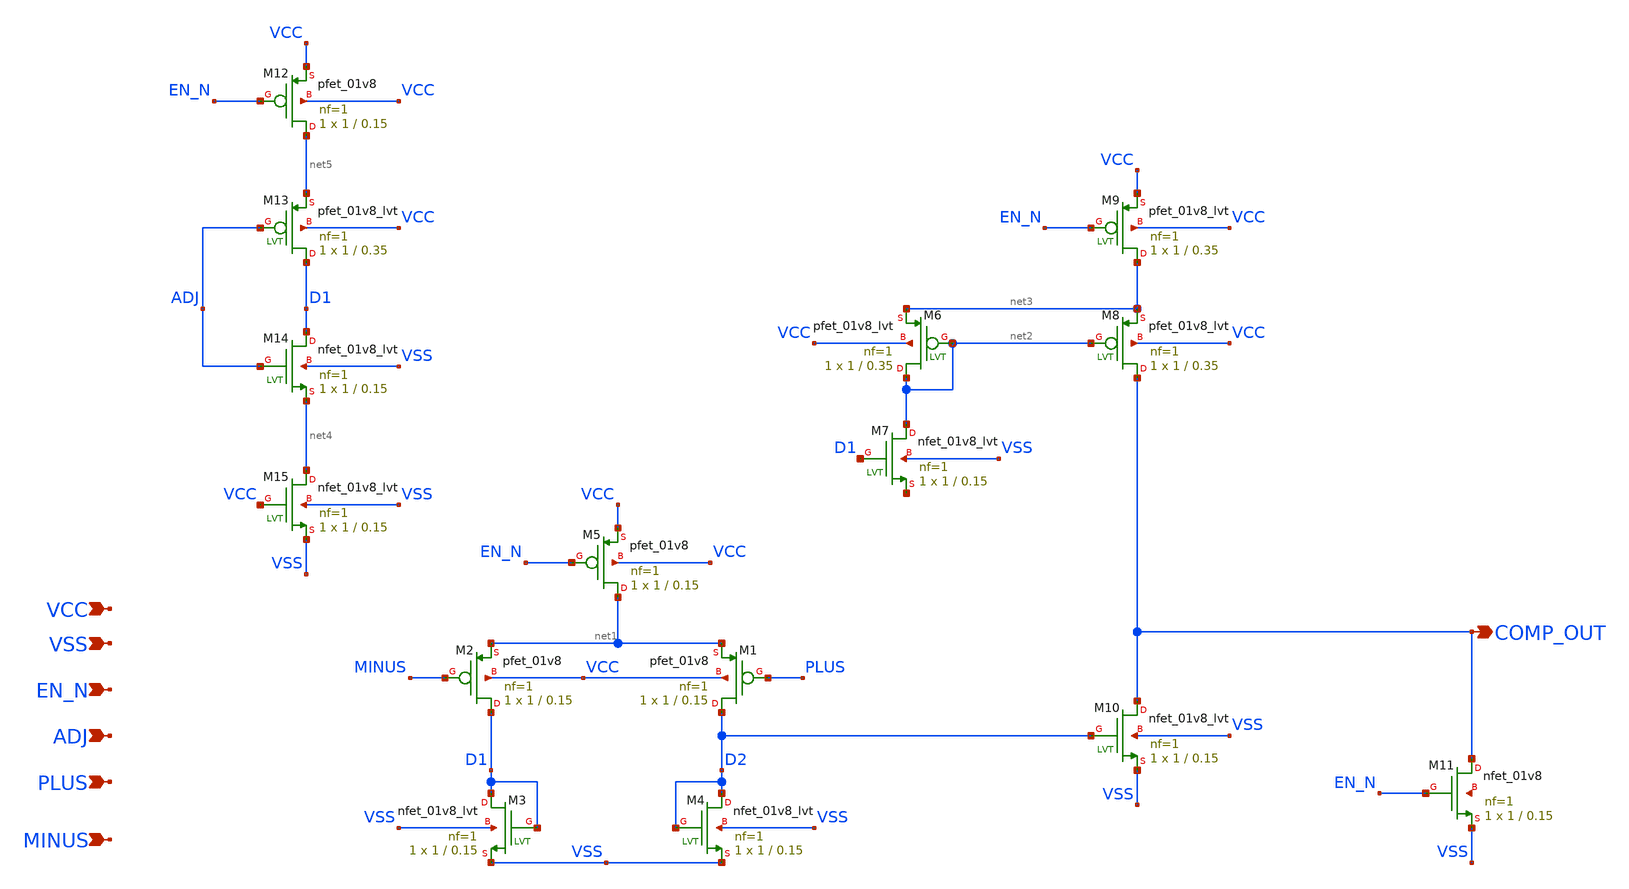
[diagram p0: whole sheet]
** sch_path: xschem/comparator.sch
**.subckt comparator VCC VSS EN_N ADJ PLUS MINUS COMP_OUT
*.ipin VCC
*.ipin VSS
*.ipin EN_N
*.ipin ADJ
*.ipin PLUS
*.ipin MINUS
*.opin COMP_OUT
XM1 D2 PLUS net1 VCC sky130_fd_pr__pfet_01v8 L=0.15 W=1 nf=1 ad='int((nf+1)/2) * W/nf * 0.29' as='int((nf+2)/2) * W/nf * 0.29'
+ pd='2*int((nf+1)/2) * (W/nf + 0.29)' ps='2*int((nf+2)/2) * (W/nf + 0.29)' nrd='0.29 / W' nrs='0.29 / W'
+ sa=0 sb=0 sd=0 mult=1 m=1
XM2 D1 MINUS net1 VCC sky130_fd_pr__pfet_01v8 L=0.15 W=1 nf=1 ad='int((nf+1)/2) * W/nf * 0.29' as='int((nf+2)/2) * W/nf * 0.29'
+ pd='2*int((nf+1)/2) * (W/nf + 0.29)' ps='2*int((nf+2)/2) * (W/nf + 0.29)' nrd='0.29 / W' nrs='0.29 / W'
+ sa=0 sb=0 sd=0 mult=1 m=1
XM3 D1 D1 VSS VSS sky130_fd_pr__nfet_01v8_lvt L=0.15 W=1 nf=1 ad='int((nf+1)/2) * W/nf * 0.29' as='int((nf+2)/2) * W/nf * 0.29'
+ pd='2*int((nf+1)/2) * (W/nf + 0.29)' ps='2*int((nf+2)/2) * (W/nf + 0.29)' nrd='0.29 / W' nrs='0.29 / W'
+ sa=0 sb=0 sd=0 mult=1 m=1
XM4 D2 D2 VSS VSS sky130_fd_pr__nfet_01v8_lvt L=0.15 W=1 nf=1 ad='int((nf+1)/2) * W/nf * 0.29' as='int((nf+2)/2) * W/nf * 0.29'
+ pd='2*int((nf+1)/2) * (W/nf + 0.29)' ps='2*int((nf+2)/2) * (W/nf + 0.29)' nrd='0.29 / W' nrs='0.29 / W'
+ sa=0 sb=0 sd=0 mult=1 m=1
XM5 net1 EN_N VCC VCC sky130_fd_pr__pfet_01v8 L=0.15 W=1 nf=1 ad='int((nf+1)/2) * W/nf * 0.29' as='int((nf+2)/2) * W/nf * 0.29'
+ pd='2*int((nf+1)/2) * (W/nf + 0.29)' ps='2*int((nf+2)/2) * (W/nf + 0.29)' nrd='0.29 / W' nrs='0.29 / W'
+ sa=0 sb=0 sd=0 mult=1 m=1
XM6 net2 net2 net3 VCC sky130_fd_pr__pfet_01v8_lvt L=0.35 W=1 nf=1 ad='int((nf+1)/2) * W/nf * 0.29' as='int((nf+2)/2) * W/nf * 0.29'
+ pd='2*int((nf+1)/2) * (W/nf + 0.29)' ps='2*int((nf+2)/2) * (W/nf + 0.29)' nrd='0.29 / W' nrs='0.29 / W'
+ sa=0 sb=0 sd=0 mult=1 m=1
XM7 net2 D1 net6 VSS sky130_fd_pr__nfet_01v8_lvt L=0.15 W=1 nf=1 ad='int((nf+1)/2) * W/nf * 0.29' as='int((nf+2)/2) * W/nf * 0.29'
+ pd='2*int((nf+1)/2) * (W/nf + 0.29)' ps='2*int((nf+2)/2) * (W/nf + 0.29)' nrd='0.29 / W' nrs='0.29 / W'
+ sa=0 sb=0 sd=0 mult=1 m=1
XM8 COMP_OUT net2 net3 VCC sky130_fd_pr__pfet_01v8_lvt L=0.35 W=1 nf=1 ad='int((nf+1)/2) * W/nf * 0.29'
+ as='int((nf+2)/2) * W/nf * 0.29' pd='2*int((nf+1)/2) * (W/nf + 0.29)' ps='2*int((nf+2)/2) * (W/nf + 0.29)'
+ nrd='0.29 / W' nrs='0.29 / W' sa=0 sb=0 sd=0 mult=1 m=1
XM9 net3 EN_N VCC VCC sky130_fd_pr__pfet_01v8_lvt L=0.35 W=1 nf=1 ad='int((nf+1)/2) * W/nf * 0.29' as='int((nf+2)/2) * W/nf * 0.29'
+ pd='2*int((nf+1)/2) * (W/nf + 0.29)' ps='2*int((nf+2)/2) * (W/nf + 0.29)' nrd='0.29 / W' nrs='0.29 / W'
+ sa=0 sb=0 sd=0 mult=1 m=1
XM10 COMP_OUT D2 VSS VSS sky130_fd_pr__nfet_01v8_lvt L=0.15 W=1 nf=1 ad='int((nf+1)/2) * W/nf * 0.29'
+ as='int((nf+2)/2) * W/nf * 0.29' pd='2*int((nf+1)/2) * (W/nf + 0.29)' ps='2*int((nf+2)/2) * (W/nf + 0.29)'
+ nrd='0.29 / W' nrs='0.29 / W' sa=0 sb=0 sd=0 mult=1 m=1
XM11 COMP_OUT EN_N VSS net7 sky130_fd_pr__nfet_01v8 L=0.15 W=1 nf=1 ad='int((nf+1)/2) * W/nf * 0.29'
+ as='int((nf+2)/2) * W/nf * 0.29' pd='2*int((nf+1)/2) * (W/nf + 0.29)' ps='2*int((nf+2)/2) * (W/nf + 0.29)'
+ nrd='0.29 / W' nrs='0.29 / W' sa=0 sb=0 sd=0 mult=1 m=1
XM12 net5 EN_N VCC VCC sky130_fd_pr__pfet_01v8 L=0.15 W=1 nf=1 ad='int((nf+1)/2) * W/nf * 0.29' as='int((nf+2)/2) * W/nf * 0.29'
+ pd='2*int((nf+1)/2) * (W/nf + 0.29)' ps='2*int((nf+2)/2) * (W/nf + 0.29)' nrd='0.29 / W' nrs='0.29 / W'
+ sa=0 sb=0 sd=0 mult=1 m=1
XM13 D1 ADJ net5 VCC sky130_fd_pr__pfet_01v8_lvt L=0.35 W=1 nf=1 ad='int((nf+1)/2) * W/nf * 0.29' as='int((nf+2)/2) * W/nf * 0.29'
+ pd='2*int((nf+1)/2) * (W/nf + 0.29)' ps='2*int((nf+2)/2) * (W/nf + 0.29)' nrd='0.29 / W' nrs='0.29 / W'
+ sa=0 sb=0 sd=0 mult=1 m=1
XM14 D1 ADJ net4 VSS sky130_fd_pr__nfet_01v8_lvt L=0.15 W=1 nf=1 ad='int((nf+1)/2) * W/nf * 0.29' as='int((nf+2)/2) * W/nf * 0.29'
+ pd='2*int((nf+1)/2) * (W/nf + 0.29)' ps='2*int((nf+2)/2) * (W/nf + 0.29)' nrd='0.29 / W' nrs='0.29 / W'
+ sa=0 sb=0 sd=0 mult=1 m=1
XM15 net4 VCC VSS VSS sky130_fd_pr__nfet_01v8_lvt L=0.15 W=1 nf=1 ad='int((nf+1)/2) * W/nf * 0.29' as='int((nf+2)/2) * W/nf * 0.29'
+ pd='2*int((nf+1)/2) * (W/nf + 0.29)' ps='2*int((nf+2)/2) * (W/nf + 0.29)' nrd='0.29 / W' nrs='0.29 / W'
+ sa=0 sb=0 sd=0 mult=1 m=1
**.ends
.end
